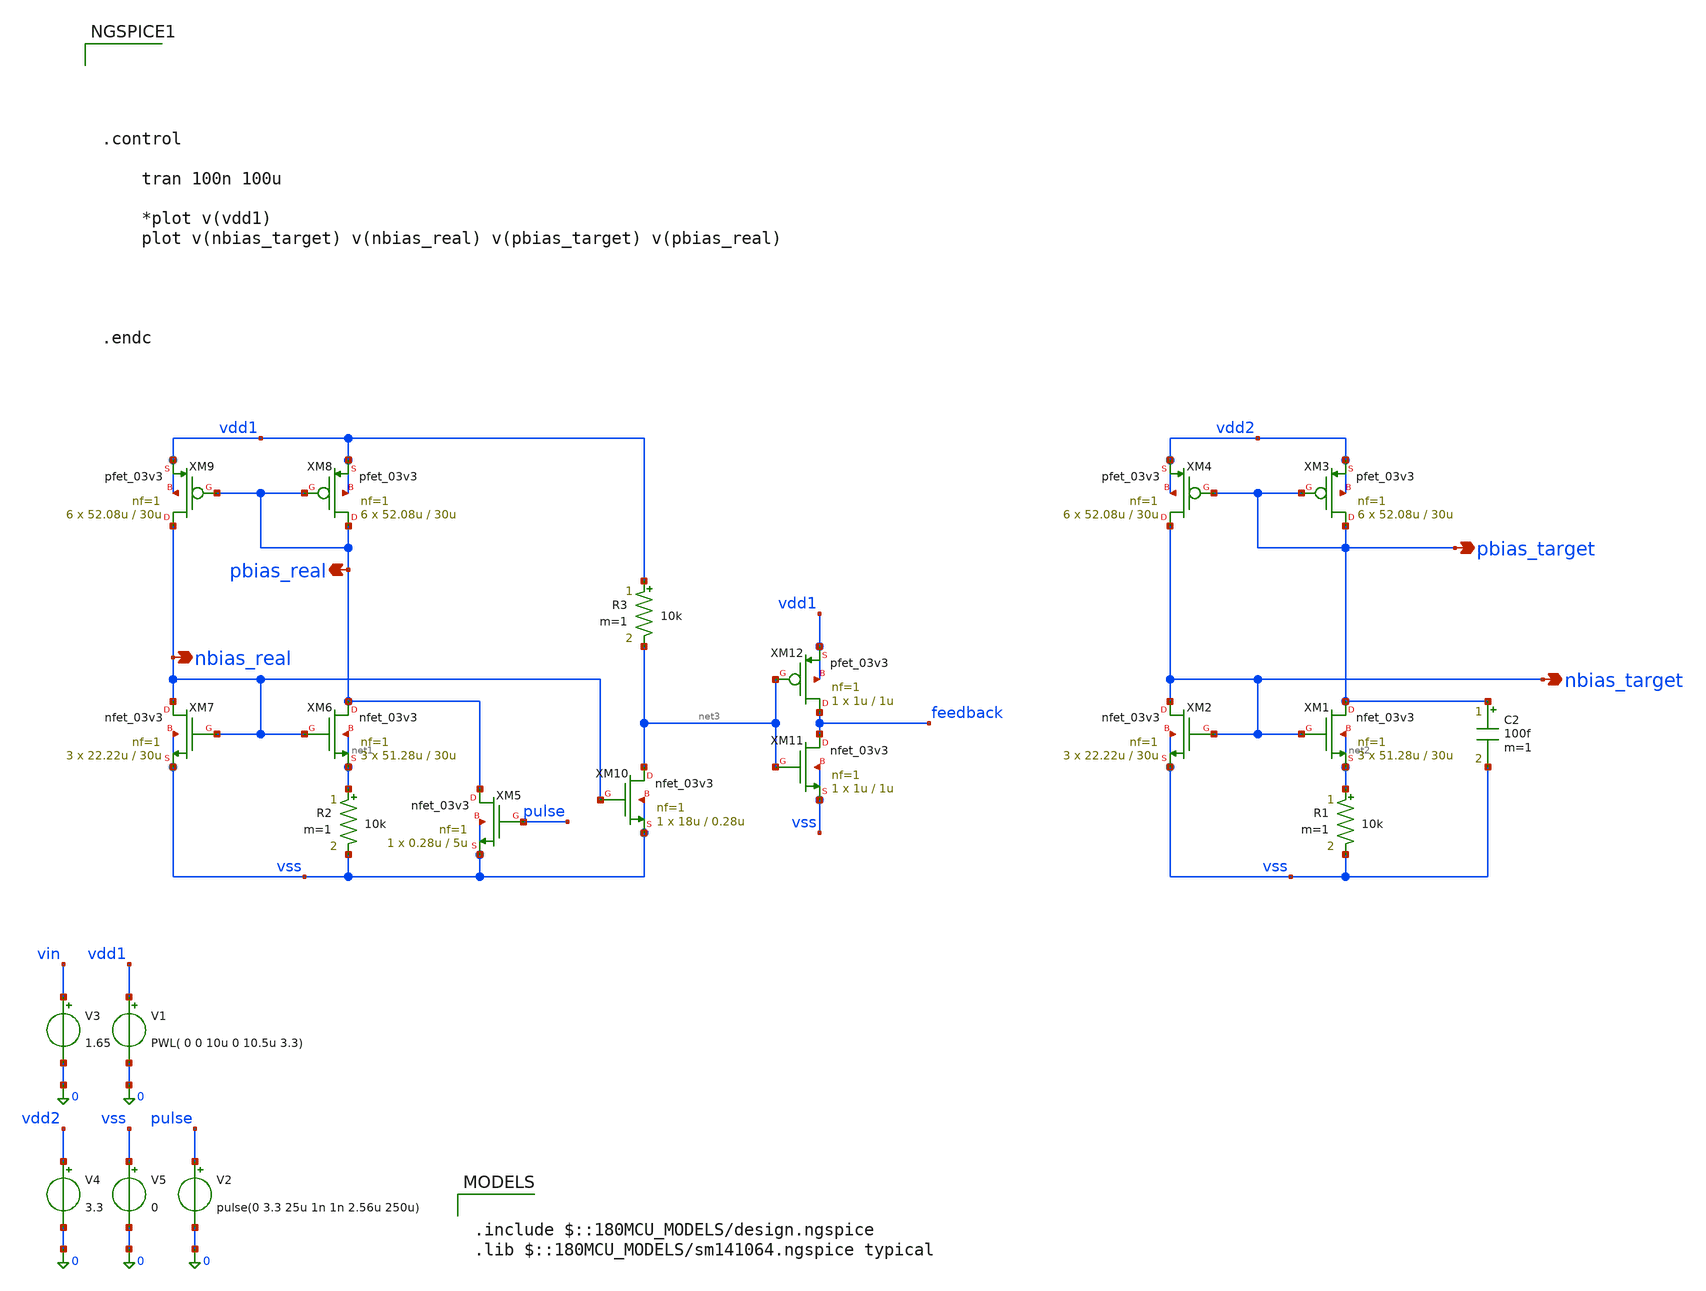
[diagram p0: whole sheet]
** sch_path: simulation/testbench_analog/untitled-13.sch
**.subckt untitled-13 pbias_real nbias_real pbias_target nbias_target
*.opin pbias_real
*.opin nbias_real
*.opin pbias_target
*.opin nbias_target
V1 vdd1 0 PWL( 0 0 10u 0 10.5u 3.3)
V3 vin 0 1.65
XM6 pbias_real nbias_real net1 net1 nfet_03v3 L=30u W=51.28u nf=1 ad='int((nf+1)/2) * W/nf * 0.18u' as='int((nf+2)/2) * W/nf * 0.18u'
+ pd='2*int((nf+1)/2) * (W/nf + 0.18u)' ps='2*int((nf+2)/2) * (W/nf + 0.18u)' nrd='0.18u / W' nrs='0.18u / W'
+ sa=0 sb=0 sd=0 m=3
XM7 nbias_real nbias_real vss vss nfet_03v3 L=30u W=22.22u nf=1 ad='int((nf+1)/2) * W/nf * 0.18u' as='int((nf+2)/2) * W/nf * 0.18u'
+ pd='2*int((nf+1)/2) * (W/nf + 0.18u)' ps='2*int((nf+2)/2) * (W/nf + 0.18u)' nrd='0.18u / W' nrs='0.18u / W'
+ sa=0 sb=0 sd=0 m=3
XM8 pbias_real pbias_real vdd1 vdd1 pfet_03v3 L=30u W=52.08u nf=1 ad='int((nf+1)/2) * W/nf * 0.18u' as='int((nf+2)/2) * W/nf * 0.18u'
+ pd='2*int((nf+1)/2) * (W/nf + 0.18u)' ps='2*int((nf+2)/2) * (W/nf + 0.18u)' nrd='0.18u / W' nrs='0.18u / W'
+ sa=0 sb=0 sd=0 m=6
XM9 nbias_real pbias_real vdd1 vdd1 pfet_03v3 L=30u W=52.08u nf=1 ad='int((nf+1)/2) * W/nf * 0.18u' as='int((nf+2)/2) * W/nf * 0.18u'
+ pd='2*int((nf+1)/2) * (W/nf + 0.18u)' ps='2*int((nf+2)/2) * (W/nf + 0.18u)' nrd='0.18u / W' nrs='0.18u / W'
+ sa=0 sb=0 sd=0 m=6
R2 net1 vss 10k m=1
V4 vdd2 0 3.3
V5 vss 0 0
XM1 pbias_target nbias_target net2 net2 nfet_03v3 L=30u W=51.28u nf=1 ad='int((nf+1)/2) * W/nf * 0.18u'
+ as='int((nf+2)/2) * W/nf * 0.18u' pd='2*int((nf+1)/2) * (W/nf + 0.18u)' ps='2*int((nf+2)/2) * (W/nf + 0.18u)'
+ nrd='0.18u / W' nrs='0.18u / W' sa=0 sb=0 sd=0 m=3
XM2 nbias_target nbias_target vss vss nfet_03v3 L=30u W=22.22u nf=1 ad='int((nf+1)/2) * W/nf * 0.18u'
+ as='int((nf+2)/2) * W/nf * 0.18u' pd='2*int((nf+1)/2) * (W/nf + 0.18u)' ps='2*int((nf+2)/2) * (W/nf + 0.18u)'
+ nrd='0.18u / W' nrs='0.18u / W' sa=0 sb=0 sd=0 m=3
XM3 pbias_target pbias_target vdd2 vdd2 pfet_03v3 L=30u W=52.08u nf=1 ad='int((nf+1)/2) * W/nf * 0.18u'
+ as='int((nf+2)/2) * W/nf * 0.18u' pd='2*int((nf+1)/2) * (W/nf + 0.18u)' ps='2*int((nf+2)/2) * (W/nf + 0.18u)'
+ nrd='0.18u / W' nrs='0.18u / W' sa=0 sb=0 sd=0 m=6
XM4 nbias_target pbias_target vdd2 vdd2 pfet_03v3 L=30u W=52.08u nf=1 ad='int((nf+1)/2) * W/nf * 0.18u'
+ as='int((nf+2)/2) * W/nf * 0.18u' pd='2*int((nf+1)/2) * (W/nf + 0.18u)' ps='2*int((nf+2)/2) * (W/nf + 0.18u)'
+ nrd='0.18u / W' nrs='0.18u / W' sa=0 sb=0 sd=0 m=6
R1 net2 vss 10k m=1
C2 pbias_target vss 100f m=1
XM5 pbias_real pulse vss vss nfet_03v3 L=5u W=0.28u nf=1 ad='int((nf+1)/2) * W/nf * 0.18u' as='int((nf+2)/2) * W/nf * 0.18u'
+ pd='2*int((nf+1)/2) * (W/nf + 0.18u)' ps='2*int((nf+2)/2) * (W/nf + 0.18u)' nrd='0.18u / W' nrs='0.18u / W'
+ sa=0 sb=0 sd=0 m=1
V2 pulse 0 pulse(0 3.3 25u 1n 1n 2.56u 250u)
XM10 net3 nbias_real vss vss nfet_03v3 L=0.28u W=18u nf=1 ad='int((nf+1)/2) * W/nf * 0.18u' as='int((nf+2)/2) * W/nf * 0.18u'
+ pd='2*int((nf+1)/2) * (W/nf + 0.18u)' ps='2*int((nf+2)/2) * (W/nf + 0.18u)' nrd='0.18u / W' nrs='0.18u / W'
+ sa=0 sb=0 sd=0 m=1
R3 vdd1 net3 10k m=1
XM11 feedback net3 vss vss nfet_03v3 L=1u W=1u nf=1 ad='int((nf+1)/2) * W/nf * 0.18u' as='int((nf+2)/2) * W/nf * 0.18u'
+ pd='2*int((nf+1)/2) * (W/nf + 0.18u)' ps='2*int((nf+2)/2) * (W/nf + 0.18u)' nrd='0.18u / W' nrs='0.18u / W'
+ sa=0 sb=0 sd=0 m=1
XM12 feedback net3 vdd1 vdd1 pfet_03v3 L=1u W=1u nf=1 ad='int((nf+1)/2) * W/nf * 0.18u' as='int((nf+2)/2) * W/nf * 0.18u'
+ pd='2*int((nf+1)/2) * (W/nf + 0.18u)' ps='2*int((nf+2)/2) * (W/nf + 0.18u)' nrd='0.18u / W' nrs='0.18u / W'
+ sa=0 sb=0 sd=0 m=1
**** begin user architecture code

.include $::180MCU_MODELS/design.ngspice
.lib $::180MCU_MODELS/sm141064.ngspice typical






.control

	tran 100n 100u

	*plot v(vdd1)
	plot v(nbias_target) v(nbias_real) v(pbias_target) v(pbias_real)




.endc


**** end user architecture code
**.ends
.end
